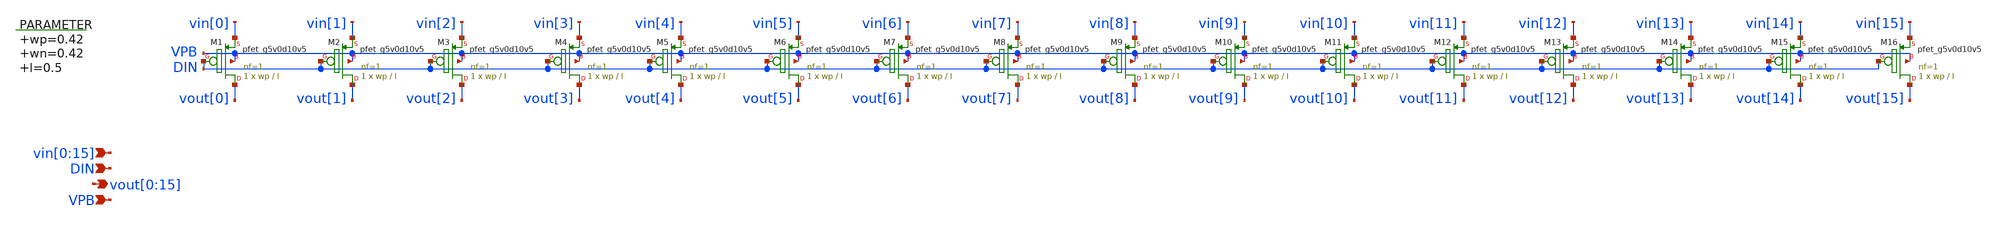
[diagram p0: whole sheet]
** sch_path: xschem/vselector_16b_1v_pmos.sch
**.subckt vselector_16b_1v_pmos
*+ vin[0],vin[1],vin[2],vin[3],vin[4],vin[5],vin[6],vin[7],vin[8],vin[9],vin[10],vin[11],vin[12],vin[13],vin[14],vin[15]
*+ vout[0],vout[1],vout[2],vout[3],vout[4],vout[5],vout[6],vout[7],vout[8],vout[9],vout[10],vout[11],vout[12],vout[13],vout[14],vout[15] VPB DIN
*.ipin
*+ vin[0],vin[1],vin[2],vin[3],vin[4],vin[5],vin[6],vin[7],vin[8],vin[9],vin[10],vin[11],vin[12],vin[13],vin[14],vin[15]
*.opin
*+ vout[0],vout[1],vout[2],vout[3],vout[4],vout[5],vout[6],vout[7],vout[8],vout[9],vout[10],vout[11],vout[12],vout[13],vout[14],vout[15]
*.ipin VPB
*.ipin DIN
.param wp=0.42 wn=0.42 l=0.5

XM1 vout[0] DIN vin[0] VPB sky130_fd_pr__pfet_g5v0d10v5 L=l W=wp nf=1 ad='int((nf+1)/2) * W/nf * 0.29'
+ as='int((nf+2)/2) * W/nf * 0.29' pd='2*int((nf+1)/2) * (W/nf + 0.29)' ps='2*int((nf+2)/2) * (W/nf + 0.29)'
+ nrd='0.29 / W' nrs='0.29 / W' sa=0 sb=0 sd=0 mult=1 m=1
XM2 vout[1] DIN vin[1] VPB sky130_fd_pr__pfet_g5v0d10v5 L=l W=wp nf=1 ad='int((nf+1)/2) * W/nf * 0.29'
+ as='int((nf+2)/2) * W/nf * 0.29' pd='2*int((nf+1)/2) * (W/nf + 0.29)' ps='2*int((nf+2)/2) * (W/nf + 0.29)'
+ nrd='0.29 / W' nrs='0.29 / W' sa=0 sb=0 sd=0 mult=1 m=1
XM3 vout[2] DIN vin[2] VPB sky130_fd_pr__pfet_g5v0d10v5 L=l W=wp nf=1 ad='int((nf+1)/2) * W/nf * 0.29'
+ as='int((nf+2)/2) * W/nf * 0.29' pd='2*int((nf+1)/2) * (W/nf + 0.29)' ps='2*int((nf+2)/2) * (W/nf + 0.29)'
+ nrd='0.29 / W' nrs='0.29 / W' sa=0 sb=0 sd=0 mult=1 m=1
XM4 vout[3] DIN vin[3] VPB sky130_fd_pr__pfet_g5v0d10v5 L=l W=wp nf=1 ad='int((nf+1)/2) * W/nf * 0.29'
+ as='int((nf+2)/2) * W/nf * 0.29' pd='2*int((nf+1)/2) * (W/nf + 0.29)' ps='2*int((nf+2)/2) * (W/nf + 0.29)'
+ nrd='0.29 / W' nrs='0.29 / W' sa=0 sb=0 sd=0 mult=1 m=1
XM5 vout[4] DIN vin[4] VPB sky130_fd_pr__pfet_g5v0d10v5 L=l W=wp nf=1 ad='int((nf+1)/2) * W/nf * 0.29'
+ as='int((nf+2)/2) * W/nf * 0.29' pd='2*int((nf+1)/2) * (W/nf + 0.29)' ps='2*int((nf+2)/2) * (W/nf + 0.29)'
+ nrd='0.29 / W' nrs='0.29 / W' sa=0 sb=0 sd=0 mult=1 m=1
XM6 vout[5] DIN vin[5] VPB sky130_fd_pr__pfet_g5v0d10v5 L=l W=wp nf=1 ad='int((nf+1)/2) * W/nf * 0.29'
+ as='int((nf+2)/2) * W/nf * 0.29' pd='2*int((nf+1)/2) * (W/nf + 0.29)' ps='2*int((nf+2)/2) * (W/nf + 0.29)'
+ nrd='0.29 / W' nrs='0.29 / W' sa=0 sb=0 sd=0 mult=1 m=1
XM7 vout[6] DIN vin[6] VPB sky130_fd_pr__pfet_g5v0d10v5 L=l W=wp nf=1 ad='int((nf+1)/2) * W/nf * 0.29'
+ as='int((nf+2)/2) * W/nf * 0.29' pd='2*int((nf+1)/2) * (W/nf + 0.29)' ps='2*int((nf+2)/2) * (W/nf + 0.29)'
+ nrd='0.29 / W' nrs='0.29 / W' sa=0 sb=0 sd=0 mult=1 m=1
XM8 vout[7] DIN vin[7] VPB sky130_fd_pr__pfet_g5v0d10v5 L=l W=wp nf=1 ad='int((nf+1)/2) * W/nf * 0.29'
+ as='int((nf+2)/2) * W/nf * 0.29' pd='2*int((nf+1)/2) * (W/nf + 0.29)' ps='2*int((nf+2)/2) * (W/nf + 0.29)'
+ nrd='0.29 / W' nrs='0.29 / W' sa=0 sb=0 sd=0 mult=1 m=1
XM9 vout[8] DIN vin[8] VPB sky130_fd_pr__pfet_g5v0d10v5 L=l W=wp nf=1 ad='int((nf+1)/2) * W/nf * 0.29'
+ as='int((nf+2)/2) * W/nf * 0.29' pd='2*int((nf+1)/2) * (W/nf + 0.29)' ps='2*int((nf+2)/2) * (W/nf + 0.29)'
+ nrd='0.29 / W' nrs='0.29 / W' sa=0 sb=0 sd=0 mult=1 m=1
XM10 vout[9] DIN vin[9] VPB sky130_fd_pr__pfet_g5v0d10v5 L=l W=wp nf=1 ad='int((nf+1)/2) * W/nf * 0.29'
+ as='int((nf+2)/2) * W/nf * 0.29' pd='2*int((nf+1)/2) * (W/nf + 0.29)' ps='2*int((nf+2)/2) * (W/nf + 0.29)'
+ nrd='0.29 / W' nrs='0.29 / W' sa=0 sb=0 sd=0 mult=1 m=1
XM11 vout[10] DIN vin[10] VPB sky130_fd_pr__pfet_g5v0d10v5 L=l W=wp nf=1 ad='int((nf+1)/2) * W/nf * 0.29'
+ as='int((nf+2)/2) * W/nf * 0.29' pd='2*int((nf+1)/2) * (W/nf + 0.29)' ps='2*int((nf+2)/2) * (W/nf + 0.29)'
+ nrd='0.29 / W' nrs='0.29 / W' sa=0 sb=0 sd=0 mult=1 m=1
XM12 vout[11] DIN vin[11] VPB sky130_fd_pr__pfet_g5v0d10v5 L=l W=wp nf=1 ad='int((nf+1)/2) * W/nf * 0.29'
+ as='int((nf+2)/2) * W/nf * 0.29' pd='2*int((nf+1)/2) * (W/nf + 0.29)' ps='2*int((nf+2)/2) * (W/nf + 0.29)'
+ nrd='0.29 / W' nrs='0.29 / W' sa=0 sb=0 sd=0 mult=1 m=1
XM13 vout[12] DIN vin[12] VPB sky130_fd_pr__pfet_g5v0d10v5 L=l W=wp nf=1 ad='int((nf+1)/2) * W/nf * 0.29'
+ as='int((nf+2)/2) * W/nf * 0.29' pd='2*int((nf+1)/2) * (W/nf + 0.29)' ps='2*int((nf+2)/2) * (W/nf + 0.29)'
+ nrd='0.29 / W' nrs='0.29 / W' sa=0 sb=0 sd=0 mult=1 m=1
XM14 vout[13] DIN vin[13] VPB sky130_fd_pr__pfet_g5v0d10v5 L=l W=wp nf=1 ad='int((nf+1)/2) * W/nf * 0.29'
+ as='int((nf+2)/2) * W/nf * 0.29' pd='2*int((nf+1)/2) * (W/nf + 0.29)' ps='2*int((nf+2)/2) * (W/nf + 0.29)'
+ nrd='0.29 / W' nrs='0.29 / W' sa=0 sb=0 sd=0 mult=1 m=1
XM15 vout[14] DIN vin[14] VPB sky130_fd_pr__pfet_g5v0d10v5 L=l W=wp nf=1 ad='int((nf+1)/2) * W/nf * 0.29'
+ as='int((nf+2)/2) * W/nf * 0.29' pd='2*int((nf+1)/2) * (W/nf + 0.29)' ps='2*int((nf+2)/2) * (W/nf + 0.29)'
+ nrd='0.29 / W' nrs='0.29 / W' sa=0 sb=0 sd=0 mult=1 m=1
XM16 vout[15] DIN vin[15] VPB sky130_fd_pr__pfet_g5v0d10v5 L=l W=wp nf=1 ad='int((nf+1)/2) * W/nf * 0.29'
+ as='int((nf+2)/2) * W/nf * 0.29' pd='2*int((nf+1)/2) * (W/nf + 0.29)' ps='2*int((nf+2)/2) * (W/nf + 0.29)'
+ nrd='0.29 / W' nrs='0.29 / W' sa=0 sb=0 sd=0 mult=1 m=1
**.ends
.end
